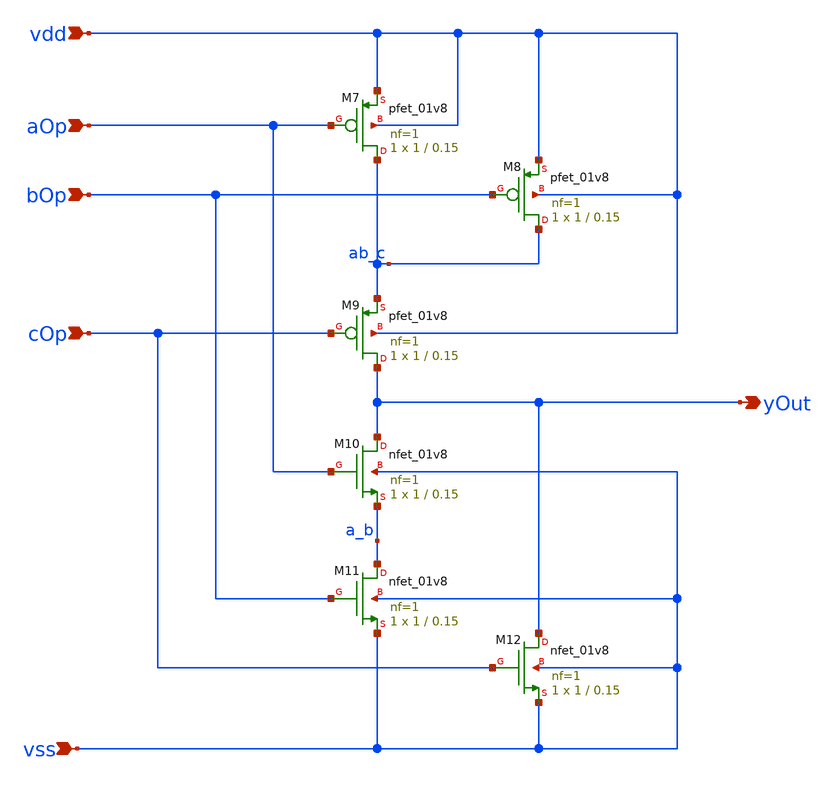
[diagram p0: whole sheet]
** sch_path: xschem/nAbPlC.sch
**.subckt nAbPlC aOp bOp cOp vdd vss yOut
*.ipin aOp
*.ipin bOp
*.ipin cOp
*.ipin vdd
*.ipin vss
*.opin yOut
XM7 ab_c aOp vdd vdd sky130_fd_pr__pfet_01v8 L=0.15 W=1 nf=1 ad='int((nf+1)/2) * W/nf * 0.29' as='int((nf+2)/2) * W/nf * 0.29'
+ pd='2*int((nf+1)/2) * (W/nf + 0.29)' ps='2*int((nf+2)/2) * (W/nf + 0.29)' nrd='0.29 / W' nrs='0.29 / W'
+ sa=0 sb=0 sd=0 mult=1 m=1
XM8 ab_c bOp vdd vdd sky130_fd_pr__pfet_01v8 L=0.15 W=1 nf=1 ad='int((nf+1)/2) * W/nf * 0.29' as='int((nf+2)/2) * W/nf * 0.29'
+ pd='2*int((nf+1)/2) * (W/nf + 0.29)' ps='2*int((nf+2)/2) * (W/nf + 0.29)' nrd='0.29 / W' nrs='0.29 / W'
+ sa=0 sb=0 sd=0 mult=1 m=1
XM9 yOut cOp ab_c vdd sky130_fd_pr__pfet_01v8 L=0.15 W=1 nf=1 ad='int((nf+1)/2) * W/nf * 0.29' as='int((nf+2)/2) * W/nf * 0.29'
+ pd='2*int((nf+1)/2) * (W/nf + 0.29)' ps='2*int((nf+2)/2) * (W/nf + 0.29)' nrd='0.29 / W' nrs='0.29 / W'
+ sa=0 sb=0 sd=0 mult=1 m=1
XM10 yOut aOp a_b vss sky130_fd_pr__nfet_01v8 L=0.15 W=1 nf=1 ad='int((nf+1)/2) * W/nf * 0.29' as='int((nf+2)/2) * W/nf * 0.29'
+ pd='2*int((nf+1)/2) * (W/nf + 0.29)' ps='2*int((nf+2)/2) * (W/nf + 0.29)' nrd='0.29 / W' nrs='0.29 / W'
+ sa=0 sb=0 sd=0 mult=1 m=1
XM11 a_b bOp vss vss sky130_fd_pr__nfet_01v8 L=0.15 W=1 nf=1 ad='int((nf+1)/2) * W/nf * 0.29' as='int((nf+2)/2) * W/nf * 0.29'
+ pd='2*int((nf+1)/2) * (W/nf + 0.29)' ps='2*int((nf+2)/2) * (W/nf + 0.29)' nrd='0.29 / W' nrs='0.29 / W'
+ sa=0 sb=0 sd=0 mult=1 m=1
XM12 yOut cOp vss vss sky130_fd_pr__nfet_01v8 L=0.15 W=1 nf=1 ad='int((nf+1)/2) * W/nf * 0.29' as='int((nf+2)/2) * W/nf * 0.29'
+ pd='2*int((nf+1)/2) * (W/nf + 0.29)' ps='2*int((nf+2)/2) * (W/nf + 0.29)' nrd='0.29 / W' nrs='0.29 / W'
+ sa=0 sb=0 sd=0 mult=1 m=1
**.ends
.end
